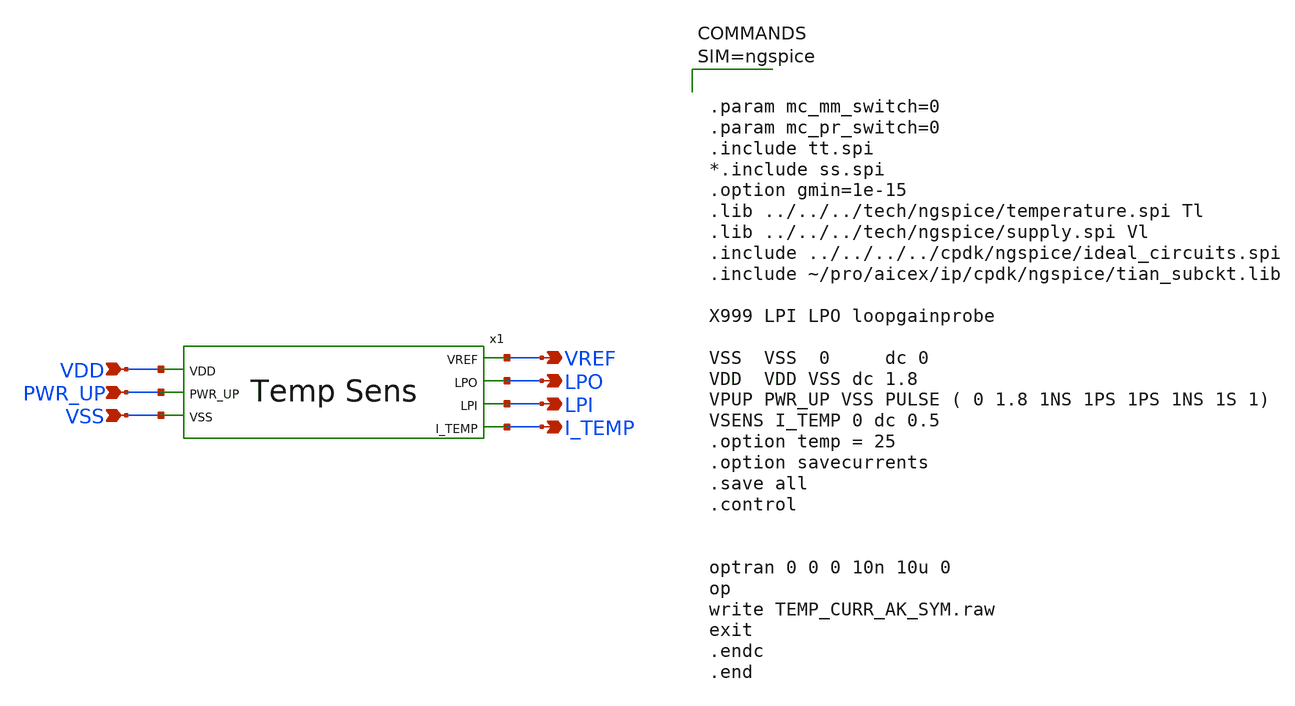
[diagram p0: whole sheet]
** sch_path: design/JNW_GR02_SKY130A/TEMP_CURR_AK_SYM.sch
**.subckt TEMP_CURR_AK_SYM VDD PWR_UP VSS VREF I_TEMP LPO LPI
*.ipin VDD
*.ipin PWR_UP
*.ipin VSS
*.opin VREF
*.opin I_TEMP
*.opin LPO
*.opin LPI
x1 VDD VREF LPO LPI PWR_UP I_TEMP VSS TEMP_CURR_AK
**** begin user architecture code



.param mc_mm_switch=0
.param mc_pr_switch=0
.include tt.spi
*.include ss.spi
.option gmin=1e-15
.lib ../../../tech/ngspice/temperature.spi Tl
.lib ../../../tech/ngspice/supply.spi Vl
.include ../../../../cpdk/ngspice/ideal_circuits.spi
.include ~/pro/aicex/ip/cpdk/ngspice/tian_subckt.lib

X999 LPI LPO loopgainprobe

VSS  VSS  0     dc 0
VDD  VDD VSS dc 1.8
VPUP PWR_UP VSS PULSE ( 0 1.8 1NS 1PS 1PS 1NS 1S 1)
VSENS I_TEMP 0 dc 0.5
.option temp = 25
.option savecurrents
.save all
.control


optran 0 0 0 10n 10u 0
op
write TEMP_CURR_AK_SYM.raw
exit
.endc
.end




**** end user architecture code
**.ends
.end
